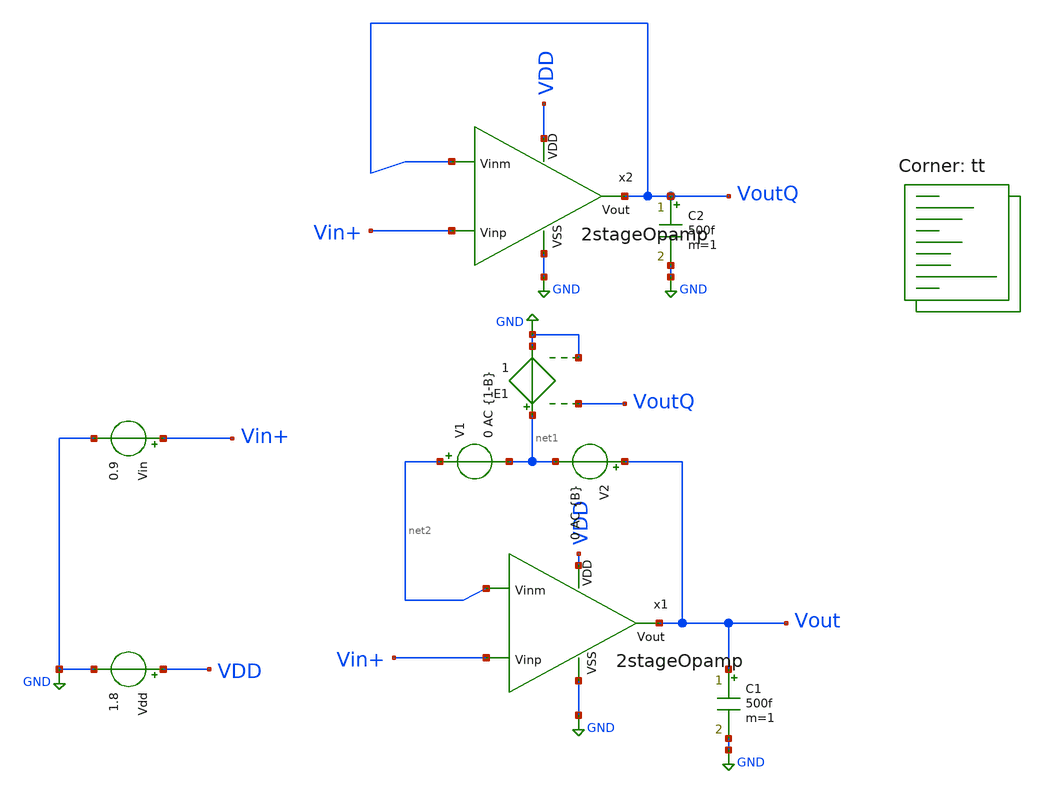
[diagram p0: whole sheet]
** sch_path: userLib/userLib/OpenLoopTB.sch
**.subckt OpenLoopTB
Vdd VDD GND 1.8
.save i(vdd)
Vin Vin+ GND 0.9
C1 Vout GND 500f m=1
V2 Vout net1 0 AC {B}
.save i(v2)
V1 net2 net1 0 AC {1-B}
.save i(v1)
C2 VoutQ GND 500f m=1
E1 net1 GND VoutQ GND 1
x1 VDD net2 Vin+ Vout GND 2stageOpamp
x2 VDD VoutQ Vin+ VoutQ GND 2stageOpamp
**** begin user architecture code
.lib $::SKYWATER_MODELS/sky130.lib.spice tt


.param B=0
.savecurrents
.control

save @m.x1.xm5.msky130_fd_pr__pfet_01v8_lvt[gm]
save @m.x1.xm5.msky130_fd_pr__pfet_01v8_lvt[gds]
save @m.x1.xm5.msky130_fd_pr__pfet_01v8_lvt[id]
save @m.x1.xm5.msky130_fd_pr__pfet_01v8_lvt[vgs] -  @m.x1.xm5.msky130_fd_pr__pfet_01v8_lvt[vth]
save @m.x1.xm5.msky130_fd_pr__pfet_01v8_lvt[vds]



save @m.x1.xm1.msky130_fd_pr__nfet_01v8[gm]
save @m.x1.xm1.msky130_fd_pr__nfet_01v8[gds]
save @m.x1.xm1.msky130_fd_pr__nfet_01v8[id]
save @m.x1.xm1.msky130_fd_pr__nfet_01v8[vgs]
save @m.x1.xm1.msky130_fd_pr__nfet_01v8[vds]

save @m.x1.xm3.msky130_fd_pr__nfet_01v8[gm]
save @m.x1.xm3.msky130_fd_pr__nfet_01v8[gds]
save @m.x1.xm3.msky130_fd_pr__nfet_01v8[id]
save @m.x1.xm3.msky130_fd_pr__nfet_01v8[vgs]
save @m.x1.xm3.msky130_fd_pr__nfet_01v8[vds]



save @m.x1.xm7.msky130_fd_pr__pfet_01v8_lvt[gm]
save @m.x1.xm7.msky130_fd_pr__pfet_01v8_lvt[gds]
save @m.x1.xm7.msky130_fd_pr__pfet_01v8_lvt[id]
save @m.x1.xm7.msky130_fd_pr__pfet_01v8_lvt[vgs]
save @m.x1.xm7.msky130_fd_pr__pfet_01v8_lvt[vds]









save @m.x1.xm9.msky130_fd_pr__pfet_01v8_lvt[gm]
save @m.x1.xm9.msky130_fd_pr__pfet_01v8_lvt[gds]
save @m.x1.xm9.msky130_fd_pr__pfet_01v8_lvt[id]
save @m.x1.xm9.msky130_fd_pr__pfet_01v8_lvt[vgs]
save @m.x1.xm9.msky130_fd_pr__pfet_01v8_lvt[vds]

save @m.x1.xm11.msky130_fd_pr__pfet_01v8_lvt[gm]
save @m.x1.xm11.msky130_fd_pr__pfet_01v8_lvt[gds]
save @m.x1.xm11.msky130_fd_pr__pfet_01v8_lvt[id]
save @m.x1.xm11.msky130_fd_pr__pfet_01v8_lvt[vgs]
save @m.x1.xm11.msky130_fd_pr__pfet_01v8_lvt[vds]




save v(Vout)

 op
 ac dec 20 1 1e12
 alterparam B=1
 reset
 ac dec 20 1 1e12
 meas ac freq_at_gain db(v(Vout))=0
 meas ac phase_at_gc ph(v(Vout)) at freq_at_gain

 setplot new
 set curplottitle=Loopgain
 let frequency = ac1.frequency

 let T = (ac1.i(V2)+ac2.i(V1))/(ac1.i(V1)+ac2.i(V2))
 let Tmag = db(T)
 let Tphase = 180 * cph(T)/pi
 let Pm = 180 + Tphase
 plot Tmag Tphase Pm xlog
 plot Tmag xlog

 plot Tphase xlog

 print @m.x1.xm5.msky130_fd_pr__pfet_01v8_lvt[gm]
 print @m.x1.xm5.msky130_fd_pr__pfet_01v8_lvt[gds]
 print @m.x1.xm5.msky130_fd_pr__pfet_01v8_lvt[id]
 print @m.x1.xm5.msky130_fd_pr__pfet_01v8_lvt[vgs]
 print @m.x1.xm5.msky130_fd_pr__pfet_01v8_lvt[vds]

print @m.x1.xm5.msky130_fd_pr__pfet_01v8_lvt[vgs] -  @m.x1.xm5.msky130_fd_pr__pfet_01v8_lvt[vth]

print @m.x1.xm1.msky130_fd_pr__pfet_01v8_lvt[vgs] -  @m.x1.xm1.msky130_fd_pr__pfet_01v8_lvt[vth]

 print @m.x1.xm7.msky130_fd_pr__pfet_01v8_lvt[gm]
 print @m.x1.xm7.msky130_fd_pr__pfet_01v8_lvt[gds]
 print @m.x1.xm7.msky130_fd_pr__pfet_01v8_lvt[id]
 print @m.x1.xm7.msky130_fd_pr__pfet_01v8_lvt[vgs]
 print @m.x1.xm7.msky130_fd_pr__pfet_01v8_lvt[vds]

 print @m.x1.xm9.msky130_fd_pr__pfet_01v8_lvt[gm]
 print @m.x1.xm9.msky130_fd_pr__pfet_01v8_lvt[gds]
 print @m.x1.xm9.msky130_fd_pr__pfet_01v8_lvt[id]
 print @m.x1.xm9.msky130_fd_pr__pfet_01v8_lvt[vgs]
 print @m.x1.xm9.msky130_fd_pr__pfet_01v8_lvt[vds]

 print @m.x1.xm11.msky130_fd_pr__pfet_01v8_lvt[gm]
 print @m.x1.xm11.msky130_fd_pr__pfet_01v8_lvt[gds]
 print @m.x1.xm11.msky130_fd_pr__pfet_01v8_lvt[id]
 print @m.x1.xm11.msky130_fd_pr__pfet_01v8_lvt[vgs]
 print @m.x1.xm11.msky130_fd_pr__pfet_01v8_lvt[vds]

 print @m.x1.xm10.msky130_fd_pr__pfet_01v8_lvt[gm]
 print @m.x1.xm10.msky130_fd_pr__pfet_01v8_lvt[gds]
 print @m.x1.xm10.msky130_fd_pr__pfet_01v8_lvt[id]
 print @m.x1.xm10.msky130_fd_pr__pfet_01v8_lvt[vgs]
 print @m.x1.xm10.msky130_fd_pr__pfet_01v8_lvt[vds]



 print @m.x1.xm1.msky130_fd_pr__nfet_01v8[gm]
 print @m.x1.xm1.msky130_fd_pr__nfet_01v8[gds]
 print @m.x1.xm1.msky130_fd_pr__nfet_01v8[id]
 print @m.x1.xm1.msky130_fd_pr__nfet_01v8[vgs] - @m.x1.xm1.msky130_fd_pr__nfet_01v8[vth]
 print @m.x1.xm1.msky130_fd_pr__nfet_01v8[vds]

 print @m.x1.xm3.msky130_fd_pr__nfet_01v8[gm]
 print @m.x1.xm3.msky130_fd_pr__nfet_01v8[gds]
 print @m.x1.xm3.msky130_fd_pr__nfet_01v8[id]
 print @m.x1.xm3.msky130_fd_pr__nfet_01v8[vgs]
 print @m.x1.xm3.msky130_fd_pr__nfet_01v8[vds]




 write OpenLoopTB.raw


.endc


**** end user architecture code
**.ends
.GLOBAL GND
.end
